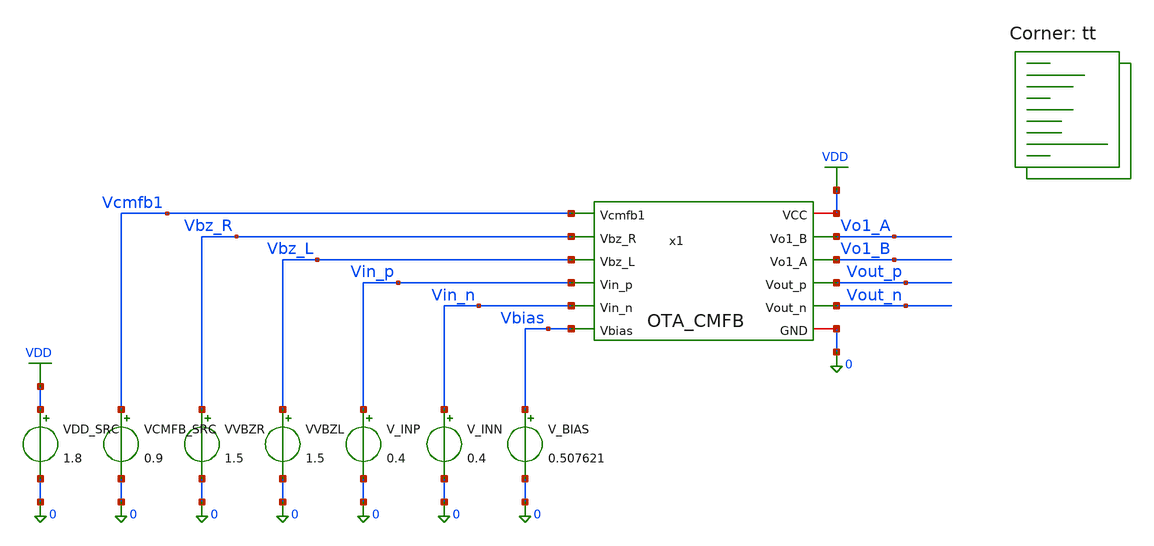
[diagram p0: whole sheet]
** sch_path: blocks/02_CMFB/sim/tb_OTA_CMFB_firststage_sign.sch
**.subckt tb_OTA_CMFB_firststage_sign
VDD_SRC VDD 0 1.8
VCMFB_SRC Vcmfb1 0 0.9
VVBZR Vbz_R 0 1.5
VVBZL Vbz_L 0 1.5
V_INP Vin_p 0 0.4
V_INN Vin_n 0 0.4
V_BIAS Vbias 0 0.507621
x1 VDD Vcmfb1 Vbz_R Vbz_L Vin_p Vin_n Vo1_A Vo1_B Vout_p Vout_n Vbias 0 OTA_CMFB
**** begin user architecture code
.lib $::SKYWATER_MODELS/sky130.lib.spice tt


.options rshunt=1e12

.control
save all

* ==========================================================
* IMPORTANT:
*
* No standalone OP command.
*
* Previous OP calculation encountered an internal singular
* node. The DC sweep itself converges correctly.
* ==========================================================


* ==========================================================
* VCMFB1 LOCAL SWEEP
*
* 0.8998 V
* 0.9000 V
* 0.9002 V
* ==========================================================

dc VCMFB_SRC 0.8998 0.9002 0.0002


* ==========================================================
* MEASURE RAW FIRST-STAGE NODES
*
* Measure real circuit nodes first.
* Common-mode values are calculated afterwards.
* This is more robust than MEAS on LET vectors.
* ==========================================================

meas dc VO1A_8998 FIND v(vo1_a) AT=0.8998
meas dc VO1A_9000 FIND v(vo1_a) AT=0.9000
meas dc VO1A_9002 FIND v(vo1_a) AT=0.9002

meas dc VO1B_8998 FIND v(vo1_b) AT=0.8998
meas dc VO1B_9000 FIND v(vo1_b) AT=0.9000
meas dc VO1B_9002 FIND v(vo1_b) AT=0.9002


* ==========================================================
* MEASURE FINAL OUTPUT NODES
* ==========================================================

meas dc VOUTP_8998 FIND v(vout_p) AT=0.8998
meas dc VOUTP_9000 FIND v(vout_p) AT=0.9000
meas dc VOUTP_9002 FIND v(vout_p) AT=0.9002

meas dc VOUTN_8998 FIND v(vout_n) AT=0.8998
meas dc VOUTN_9000 FIND v(vout_n) AT=0.9000
meas dc VOUTN_9002 FIND v(vout_n) AT=0.9002


* ==========================================================
* CALCULATE FIRST-STAGE COMMON MODE
* ==========================================================

let VO1CM_8998 = (VO1A_8998 + VO1B_8998)/2
let VO1CM_9000 = (VO1A_9000 + VO1B_9000)/2
let VO1CM_9002 = (VO1A_9002 + VO1B_9002)/2

let VO1D_8998 = VO1A_8998 - VO1B_8998
let VO1D_9000 = VO1A_9000 - VO1B_9000
let VO1D_9002 = VO1A_9002 - VO1B_9002


* ==========================================================
* CALCULATE FINAL OUTPUT COMMON MODE
* ==========================================================

let VOCM_8998 = (VOUTP_8998 + VOUTN_8998)/2
let VOCM_9000 = (VOUTP_9000 + VOUTN_9000)/2
let VOCM_9002 = (VOUTP_9002 + VOUTN_9002)/2

let VOD_8998 = VOUTP_8998 - VOUTN_8998
let VOD_9000 = VOUTP_9000 - VOUTN_9000
let VOD_9002 = VOUTP_9002 - VOUTN_9002


* ==========================================================
* CONTROL SLOPES
* ==========================================================

let DELTA_VCMFB = 0.0004

let DELTA_VO1CM = VO1CM_9002 - VO1CM_8998
let VO1_CM_SLOPE = DELTA_VO1CM / DELTA_VCMFB

let DELTA_VOCM = VOCM_9002 - VOCM_8998
let FINAL_CM_SLOPE = DELTA_VOCM / DELTA_VCMFB


* ==========================================================
* FIRST-STAGE VCMO TARGET
*
* At nominal:
*
* Vcmfb1 = 0.9000 V
*
* This is the value to use later as Vcmo for SC-CMFB.
* ==========================================================

let VCMO_FIRST_STAGE = VO1CM_9000


* ==========================================================
* PRINT FIRST-STAGE RESULTS
* ==========================================================

echo
echo ================================================
echo ===== OTA FIRST-STAGE CMFB RESULTS =============
echo ================================================

print VO1A_8998
print VO1A_9000
print VO1A_9002

print VO1B_8998
print VO1B_9000
print VO1B_9002

print VO1CM_8998
print VO1CM_9000
print VO1CM_9002

print VO1D_8998
print VO1D_9000
print VO1D_9002

print DELTA_VO1CM
print VO1_CM_SLOPE

print VCMO_FIRST_STAGE


* ==========================================================
* PRINT FINAL OUTPUT RESULTS
* ==========================================================

echo
echo ================================================
echo ===== FINAL OTA OUTPUT RESULTS =================
echo ================================================

print VOUTP_8998
print VOUTP_9000
print VOUTP_9002

print VOUTN_8998
print VOUTN_9000
print VOUTN_9002

print VOCM_8998
print VOCM_9000
print VOCM_9002

print VOD_8998
print VOD_9000
print VOD_9002

print DELTA_VOCM
print FINAL_CM_SLOPE


* ==========================================================
* WAVEFORM VECTORS
* ==========================================================

let VO1CM_TRACE = (v(vo1_a)+v(vo1_b))/2
let VOCM_TRACE  = (v(vout_p)+v(vout_n))/2


* ==========================================================
* PLOTS
* ==========================================================

plot VO1CM_TRACE
plot v(vo1_a) v(vo1_b)

plot VOCM_TRACE
plot v(vout_p) v(vout_n)

.endc


**** end user architecture code
**.ends
.GLOBAL VDD
.end
